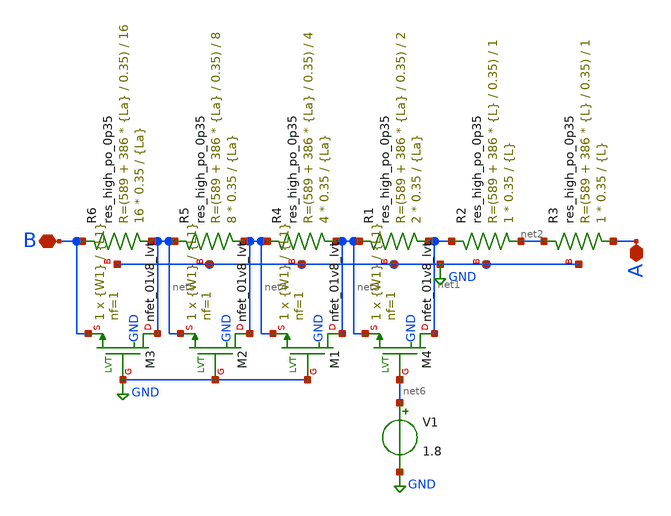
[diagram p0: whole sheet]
** sch_path: xschem/Resistor50k_1_sp.sch
**.subckt Resistor50k_1_sp A B
*.iopin A
*.iopin B
XR2 net2 net1 GND sky130_fd_pr__res_high_po_0p35 L={L} mult=1 m=1
XR3 A net2 GND sky130_fd_pr__res_high_po_0p35 L={L} mult=1 m=1
XR1 net1 net3 GND sky130_fd_pr__res_high_po_0p35 L={La} mult=2 m=2
XR4 net3 net4 GND sky130_fd_pr__res_high_po_0p35 L={La} mult=4 m=4
XR5 net4 net5 GND sky130_fd_pr__res_high_po_0p35 L={La} mult=8 m=8
XR6 net5 B GND sky130_fd_pr__res_high_po_0p35 L={La} mult=16 m=16
V1 net6 GND 1.8
XM4 net1 net6 net3 GND sky130_fd_pr__nfet_01v8_lvt L={L1} W={W1} nf=1 ad='int((nf+1)/2) * W/nf * 0.29'
+ as='int((nf+2)/2) * W/nf * 0.29' pd='2*int((nf+1)/2) * (W/nf + 0.29)' ps='2*int((nf+2)/2) * (W/nf + 0.29)'
+ nrd='0.29 / W' nrs='0.29 / W' sa=0 sb=0 sd=0 mult=1 m=1
XM1 net3 GND net4 GND sky130_fd_pr__nfet_01v8_lvt L={L1} W={W1} nf=1 ad='int((nf+1)/2) * W/nf * 0.29'
+ as='int((nf+2)/2) * W/nf * 0.29' pd='2*int((nf+1)/2) * (W/nf + 0.29)' ps='2*int((nf+2)/2) * (W/nf + 0.29)'
+ nrd='0.29 / W' nrs='0.29 / W' sa=0 sb=0 sd=0 mult=1 m=1
XM2 net4 GND net5 GND sky130_fd_pr__nfet_01v8_lvt L={L1} W={W1} nf=1 ad='int((nf+1)/2) * W/nf * 0.29'
+ as='int((nf+2)/2) * W/nf * 0.29' pd='2*int((nf+1)/2) * (W/nf + 0.29)' ps='2*int((nf+2)/2) * (W/nf + 0.29)'
+ nrd='0.29 / W' nrs='0.29 / W' sa=0 sb=0 sd=0 mult=1 m=1
XM3 net5 GND B GND sky130_fd_pr__nfet_01v8_lvt L={L1} W={W1} nf=1 ad='int((nf+1)/2) * W/nf * 0.29' as='int((nf+2)/2) * W/nf * 0.29'
+ pd='2*int((nf+1)/2) * (W/nf + 0.29)' ps='2*int((nf+2)/2) * (W/nf + 0.29)' nrd='0.29 / W' nrs='0.29 / W'
+ sa=0 sb=0 sd=0 mult=1 m=1
**** begin user architecture code


.param L=17
.param La=8.5
.param L1=1
.param W1=15


**** end user architecture code
**.ends
.GLOBAL GND
.end
